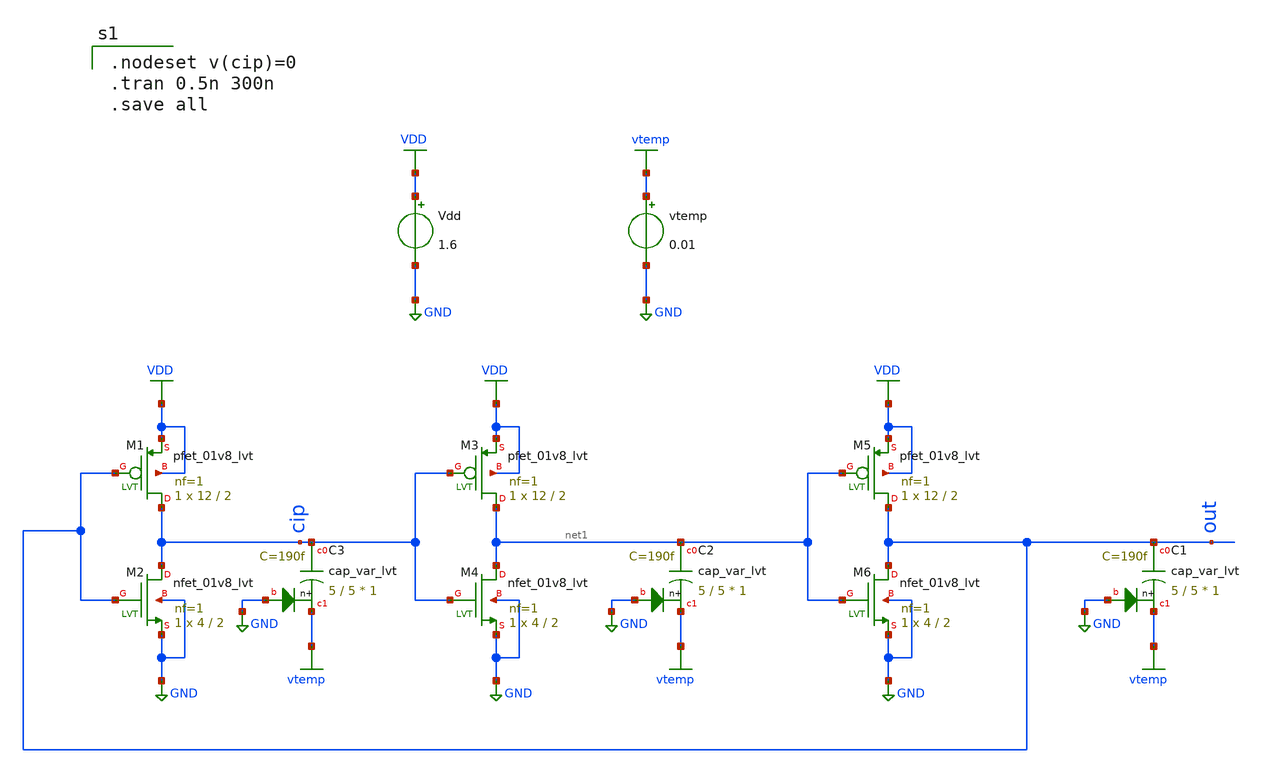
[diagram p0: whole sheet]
** sch_path: XSCHEM/ring_oscillator_design_tb.sch
**.subckt ring_oscillator_design_tb
Vdd VDD GND 1.6
XM1 cip out VDD VDD sky130_fd_pr__pfet_01v8_lvt L=2 W=12 nf=1 ad='int((nf+1)/2) * W/nf * 0.29' as='int((nf+2)/2) * W/nf * 0.29'
+ pd='2*int((nf+1)/2) * (W/nf + 0.29)' ps='2*int((nf+2)/2) * (W/nf + 0.29)' nrd='0.29 / W' nrs='0.29 / W'
+ sa=0 sb=0 sd=0 mult=1 m=1
XM2 cip out GND GND sky130_fd_pr__nfet_01v8_lvt L=2 W=4 nf=1 ad='int((nf+1)/2) * W/nf * 0.29' as='int((nf+2)/2) * W/nf * 0.29'
+ pd='2*int((nf+1)/2) * (W/nf + 0.29)' ps='2*int((nf+2)/2) * (W/nf + 0.29)' nrd='0.29 / W' nrs='0.29 / W'
+ sa=0 sb=0 sd=0 mult=1 m=1
XM3 net1 cip VDD VDD sky130_fd_pr__pfet_01v8_lvt L=2 W=12 nf=1 ad='int((nf+1)/2) * W/nf * 0.29' as='int((nf+2)/2) * W/nf * 0.29'
+ pd='2*int((nf+1)/2) * (W/nf + 0.29)' ps='2*int((nf+2)/2) * (W/nf + 0.29)' nrd='0.29 / W' nrs='0.29 / W'
+ sa=0 sb=0 sd=0 mult=1 m=1
XM4 net1 cip GND GND sky130_fd_pr__nfet_01v8_lvt L=2 W=4 nf=1 ad='int((nf+1)/2) * W/nf * 0.29' as='int((nf+2)/2) * W/nf * 0.29'
+ pd='2*int((nf+1)/2) * (W/nf + 0.29)' ps='2*int((nf+2)/2) * (W/nf + 0.29)' nrd='0.29 / W' nrs='0.29 / W'
+ sa=0 sb=0 sd=0 mult=1 m=1
XM5 out net1 VDD VDD sky130_fd_pr__pfet_01v8_lvt L=2 W=12 nf=1 ad='int((nf+1)/2) * W/nf * 0.29' as='int((nf+2)/2) * W/nf * 0.29'
+ pd='2*int((nf+1)/2) * (W/nf + 0.29)' ps='2*int((nf+2)/2) * (W/nf + 0.29)' nrd='0.29 / W' nrs='0.29 / W'
+ sa=0 sb=0 sd=0 mult=1 m=1
XM6 out net1 GND GND sky130_fd_pr__nfet_01v8_lvt L=2 W=4 nf=1 ad='int((nf+1)/2) * W/nf * 0.29' as='int((nf+2)/2) * W/nf * 0.29'
+ pd='2*int((nf+1)/2) * (W/nf + 0.29)' ps='2*int((nf+2)/2) * (W/nf + 0.29)' nrd='0.29 / W' nrs='0.29 / W'
+ sa=0 sb=0 sd=0 mult=1 m=1
XC1 out vtemp GND sky130_fd_pr__cap_var_lvt W=5 L=5 VM=1 m=1
vtemp vtemp GND 0.01
XC2 net1 vtemp GND sky130_fd_pr__cap_var_lvt W=5 L=5 VM=1 m=1
XC3 cip vtemp GND sky130_fd_pr__cap_var_lvt W=5 L=5 VM=1 m=1
**** begin user architecture code

.nodeset v(cip)=0
.tran 0.5n 300n
.save all


** opencircuitdesign pdks install
.lib $::SKYWATER_MODELS/sky130.lib.spice ff
.include /usr/local/share/pdk/sky130A/libs.ref/sky130_fd_sc_hd/spice/sky130_fd_sc_hd.spice

**** end user architecture code
**.ends
.GLOBAL GND
.GLOBAL VDD
.GLOBAL vtemp
.end
